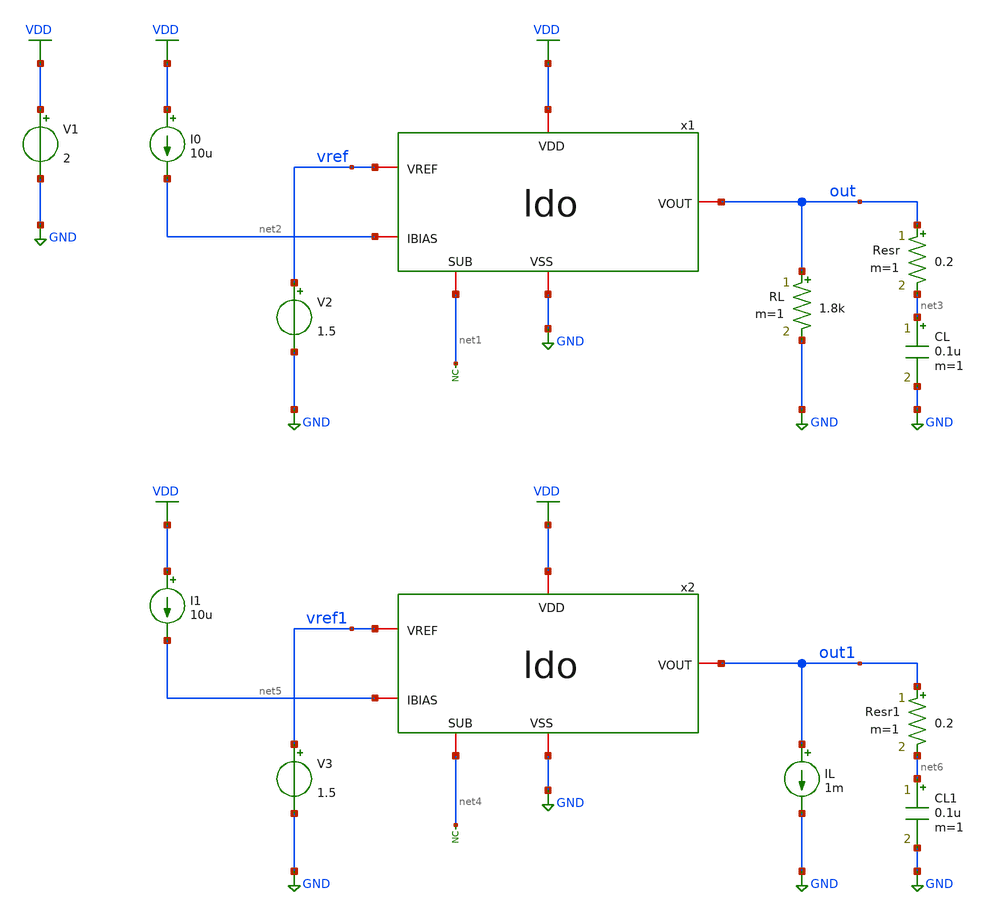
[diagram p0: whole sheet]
** sch_path: designs/libs/tb_ldo/tb_ldo/tb_ldo/tb_ldo_dc/tb_ldo_dc.sch
**.subckt tb_ldo_dc
* noconn #net1
RL out GND 1.8k m=1
V1 VDD GND 2
V2 vref GND 1.5
I0 VDD net2 10u
CL net3 GND 0.1u m=1
Resr out net3 0.2 m=1
x1 VDD vref out net2 net1 GND ldo
IL out1 GND 1m
* noconn #net4
V3 vref1 GND 1.5
I1 VDD net5 10u
CL1 net6 GND 0.1u m=1
Resr1 out1 net6 0.2 m=1
x2 VDD vref1 out1 net5 net4 GND ldo
**** begin user architecture code



.control
save all

** Dropout voltage simulation
dc V1 0 5 0.01

** Measurements
meas dc Vdd_min FIND v(vdd) WHEN v(out)=1.8 RISE=1
let Vdropout=Vdd_min-1.8
print Vdropout

** Plots
setplot dc1
let vout=v(out)
let vin=v(vdd)
plot vout vin

write tb_ldo_dc1.raw

** Line regulation simulation
dc V1 2 5 0.001

** Measurements
meas dc Vout_max MAX v(out)
meas dc Vout_min MIN v(out)
let DeltaVdd=5-2
let DeltaVout=Vout_max-Vout_min
let Line_reg=DeltaVout/DeltaVdd
print Line_reg

** Plots
setplot dc2
let vout=v(out)
plot vout

write tb_ldo_dc2.raw

** Load regulation simulation
dc IL 0 2m 0.01m

** Measurements
meas dc Vout_max MAX v(out1)
meas dc Vout_min MIN v(out1)
let DeltaVout = Vout_max-Vout_min
let DeltaIload = 0-2m
let Load_reg = abs(DeltaVout/DeltaIload)
let Load_reg_por = (DeltaVout/1.8)*100
print Load_reg
print Load_reg_por

** Plots
setplot dc3
let vout=v(out1)
plot vout

write tb_ldo_dc3.raw

.endc
* ngspice commands




.include $::180MCU_MODELS/design.ngspice
.lib $::180MCU_MODELS/sm141064.ngspice typical
.lib $::180MCU_MODELS/sm141064.ngspice cap_mim
.lib $::180MCU_MODELS/sm141064.ngspice moscap_typical
.lib $::180MCU_MODELS/sm141064.ngspice mimcap_typical
.lib $::180MCU_MODELS/sm141064.ngspice res_typical
* .lib $::180MCU_MODELS/sm141064.ngspice res_statistical
* ngspice commands

**** end user architecture code
**.ends
.GLOBAL GND
.GLOBAL VDD
.end
